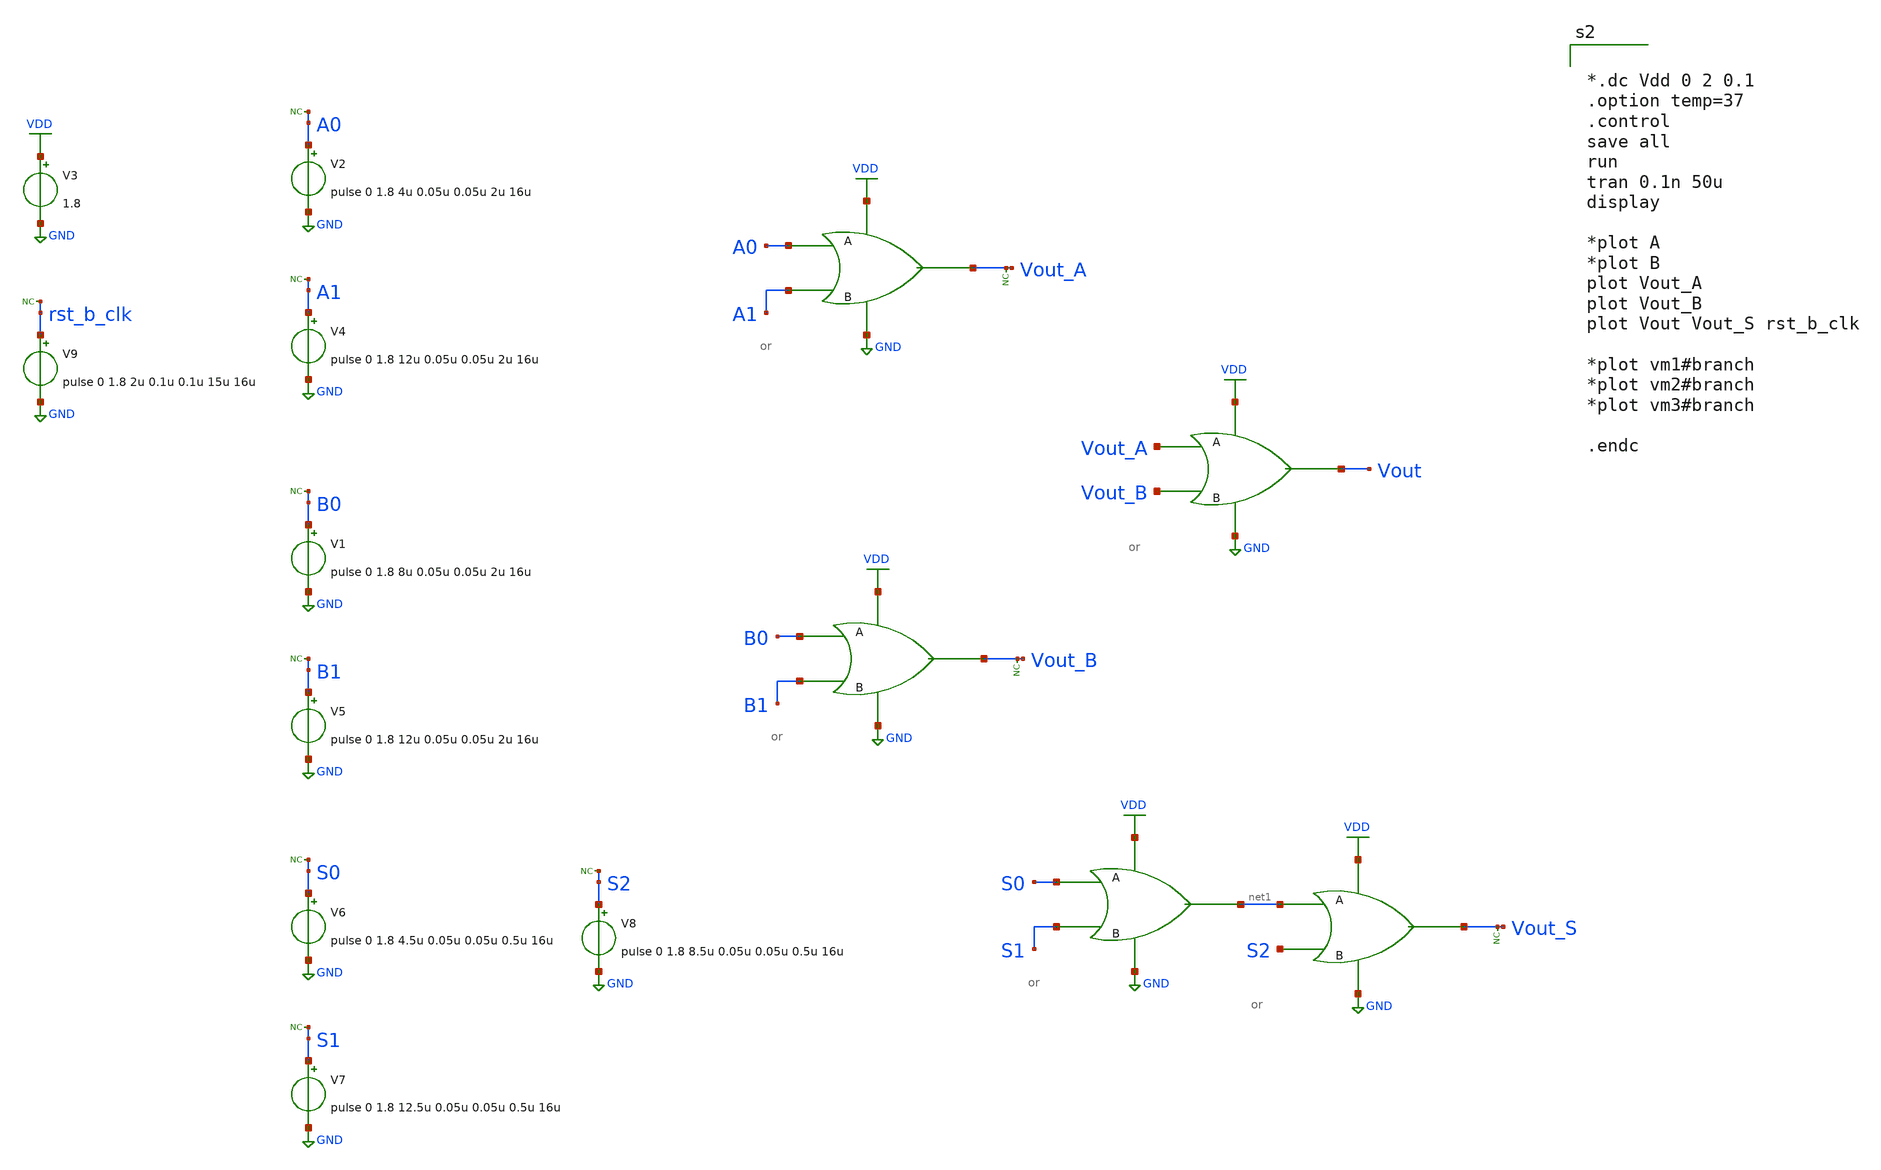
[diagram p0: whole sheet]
** sch_path: xschem/cmos_imager/row_select_clk.sch
**.subckt row_select_clk
V2 A0 GND pulse 0 1.8 4u 0.05u 0.05u 2u 16u
* noconn A0
V3 VDD GND 1.8
X1 A0 Vout_A GND VDD A1 or
* noconn Vout_A
V4 A1 GND pulse 0 1.8 12u 0.05u 0.05u 2u 16u
* noconn A1
V1 B0 GND pulse 0 1.8 8u 0.05u 0.05u 2u 16u
* noconn B0
V5 B1 GND pulse 0 1.8 12u 0.05u 0.05u 2u 16u
* noconn B1
X2 B0 Vout_B GND VDD B1 or
* noconn Vout_B
X3 Vout_A Vout GND VDD Vout_B or
V6 S0 GND pulse 0 1.8 4.5u 0.05u 0.05u 0.5u 16u
* noconn S0
V7 S1 GND pulse 0 1.8 12.5u 0.05u 0.05u 0.5u 16u
* noconn S1
V8 S2 GND pulse 0 1.8 8.5u 0.05u 0.05u 0.5u 16u
* noconn S2
X4 S0 net1 GND VDD S1 or
X5 net1 Vout_S GND VDD S2 or
* noconn Vout_S
V9 rst_b_clk GND pulse 0 1.8 2u 0.1u 0.1u 15u 16u
* noconn rst_b_clk
**** begin user architecture code

** opencircuitdesign pdks install
.lib $::SKYWATER_MODELS/sky130.lib.spice tt




*.dc Vdd 0 2 0.1
.option temp=37
.control
save all
run
tran 0.1n 50u
display

*plot A
*plot B
plot Vout_A
plot Vout_B
plot Vout Vout_S rst_b_clk

*plot vm1#branch
*plot vm2#branch
*plot vm3#branch

.endc


**** end user architecture code
**.ends
.GLOBAL GND
.GLOBAL VDD
.end
